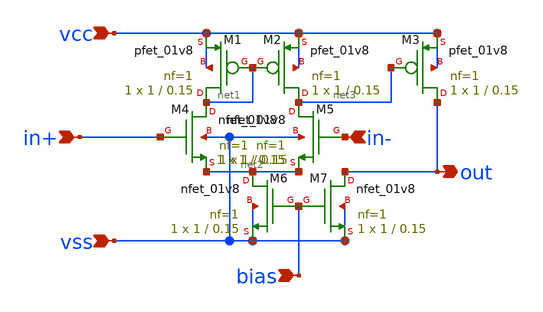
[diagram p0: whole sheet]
** sch_path: opamp.sch
**.subckt opamp in+ in- vcc vss out bias
*.ipin in+
*.ipin in-
*.ipin vcc
*.ipin vss
*.opin out
*.ipin bias
XM1 net1 net1 vcc vcc sky130_fd_pr__pfet_01v8 L=0.15 W=1 nf=1 ad='int((nf+1)/2) * W/nf * 0.29' as='int((nf+2)/2) * W/nf * 0.29'
+ pd='2*int((nf+1)/2) * (W/nf + 0.29)' ps='2*int((nf+2)/2) * (W/nf + 0.29)' nrd='0.29 / W' nrs='0.29 / W'
+ sa=0 sb=0 sd=0 mult=1 m=1
XM2 net3 net1 vcc vcc sky130_fd_pr__pfet_01v8 L=0.15 W=1 nf=1 ad='int((nf+1)/2) * W/nf * 0.29' as='int((nf+2)/2) * W/nf * 0.29'
+ pd='2*int((nf+1)/2) * (W/nf + 0.29)' ps='2*int((nf+2)/2) * (W/nf + 0.29)' nrd='0.29 / W' nrs='0.29 / W'
+ sa=0 sb=0 sd=0 mult=1 m=1
XM3 out net3 vcc vcc sky130_fd_pr__pfet_01v8 L=0.15 W=1 nf=1 ad='int((nf+1)/2) * W/nf * 0.29' as='int((nf+2)/2) * W/nf * 0.29'
+ pd='2*int((nf+1)/2) * (W/nf + 0.29)' ps='2*int((nf+2)/2) * (W/nf + 0.29)' nrd='0.29 / W' nrs='0.29 / W'
+ sa=0 sb=0 sd=0 mult=1 m=1
XM4 net1 in+ net2 vss sky130_fd_pr__nfet_01v8 L=0.15 W=1 nf=1 ad='int((nf+1)/2) * W/nf * 0.29' as='int((nf+2)/2) * W/nf * 0.29'
+ pd='2*int((nf+1)/2) * (W/nf + 0.29)' ps='2*int((nf+2)/2) * (W/nf + 0.29)' nrd='0.29 / W' nrs='0.29 / W'
+ sa=0 sb=0 sd=0 mult=1 m=1
XM5 net3 in- net2 vss sky130_fd_pr__nfet_01v8 L=0.15 W=1 nf=1 ad='int((nf+1)/2) * W/nf * 0.29' as='int((nf+2)/2) * W/nf * 0.29'
+ pd='2*int((nf+1)/2) * (W/nf + 0.29)' ps='2*int((nf+2)/2) * (W/nf + 0.29)' nrd='0.29 / W' nrs='0.29 / W'
+ sa=0 sb=0 sd=0 mult=1 m=1
XM6 net2 bias vss vss sky130_fd_pr__nfet_01v8 L=0.15 W=1 nf=1 ad='int((nf+1)/2) * W/nf * 0.29' as='int((nf+2)/2) * W/nf * 0.29'
+ pd='2*int((nf+1)/2) * (W/nf + 0.29)' ps='2*int((nf+2)/2) * (W/nf + 0.29)' nrd='0.29 / W' nrs='0.29 / W'
+ sa=0 sb=0 sd=0 mult=1 m=1
XM7 out bias vss vss sky130_fd_pr__nfet_01v8 L=0.15 W=1 nf=1 ad='int((nf+1)/2) * W/nf * 0.29' as='int((nf+2)/2) * W/nf * 0.29'
+ pd='2*int((nf+1)/2) * (W/nf + 0.29)' ps='2*int((nf+2)/2) * (W/nf + 0.29)' nrd='0.29 / W' nrs='0.29 / W'
+ sa=0 sb=0 sd=0 mult=1 m=1
**.ends
.end
